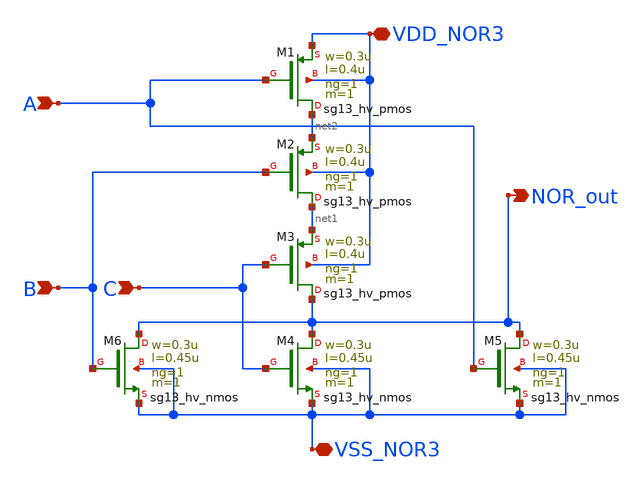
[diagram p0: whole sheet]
** sch_path: circuit_files/sarADC/nor3.sch
**.subckt nor3 VDD_NOR3 VSS_NOR3 NOR_out A B C
*.iopin VDD_NOR3
*.iopin VSS_NOR3
*.opin NOR_out
*.ipin A
*.ipin B
*.ipin C
XM1 net2 A VDD_NOR3 VDD_NOR3 sg13_hv_pmos w=0.3u l=0.4u ng=1 m=1 mm_ok=1
XM2 net1 B net2 VDD_NOR3 sg13_hv_pmos w=0.3u l=0.4u ng=1 m=1 mm_ok=1
XM3 NOR_out C net1 VDD_NOR3 sg13_hv_pmos w=0.3u l=0.4u ng=1 m=1 mm_ok=1
XM4 NOR_out C VSS_NOR3 VSS_NOR3 sg13_hv_nmos w=0.3u l=0.45u ng=1 m=1 mm_ok=1
XM5 NOR_out A VSS_NOR3 VSS_NOR3 sg13_hv_nmos w=0.3u l=0.45u ng=1 m=1 mm_ok=1
XM6 NOR_out B VSS_NOR3 VSS_NOR3 sg13_hv_nmos w=0.3u l=0.45u ng=1 m=1 mm_ok=1
**.ends
.end
